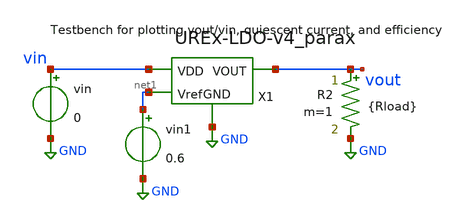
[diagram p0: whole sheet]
** sch_path: xschem/testbenches/postlayout/VoutvsVin-v4-postlayout.sch
**.subckt VoutvsVin-v4-postlayout
vin vin GND 0
R2 vout GND {Rload} m=1
X1 vin vout GND net1 UREx-LDO-v4_parax
vin1 net1 GND 0.6
**** begin user architecture code



.lib /usr/local/share/pdk/sky130A/libs.tech/ngspice/sky130.lib.spice tt
.param Rload = 20
.dc vin 0.5 5 0.1
*.tran 5u 10m

.control
run
let Rload = 20
let iout = vout/Rload
let iq = (-i(vin))-iout
let eff = (iout*vout*100)/((iout+iq)*vin)

plot v(vout)
plot iq
plot eff

.endc


**** end user architecture code
**.ends

* expanding   symbol:  UREx-LDO-v4_parax.sym # of pins=4
** sym_path: xschem/UREx-LDO-v4.sym
.include [file normalize UREx-LDO-v4_parax.spice]
.GLOBAL GND
.end
